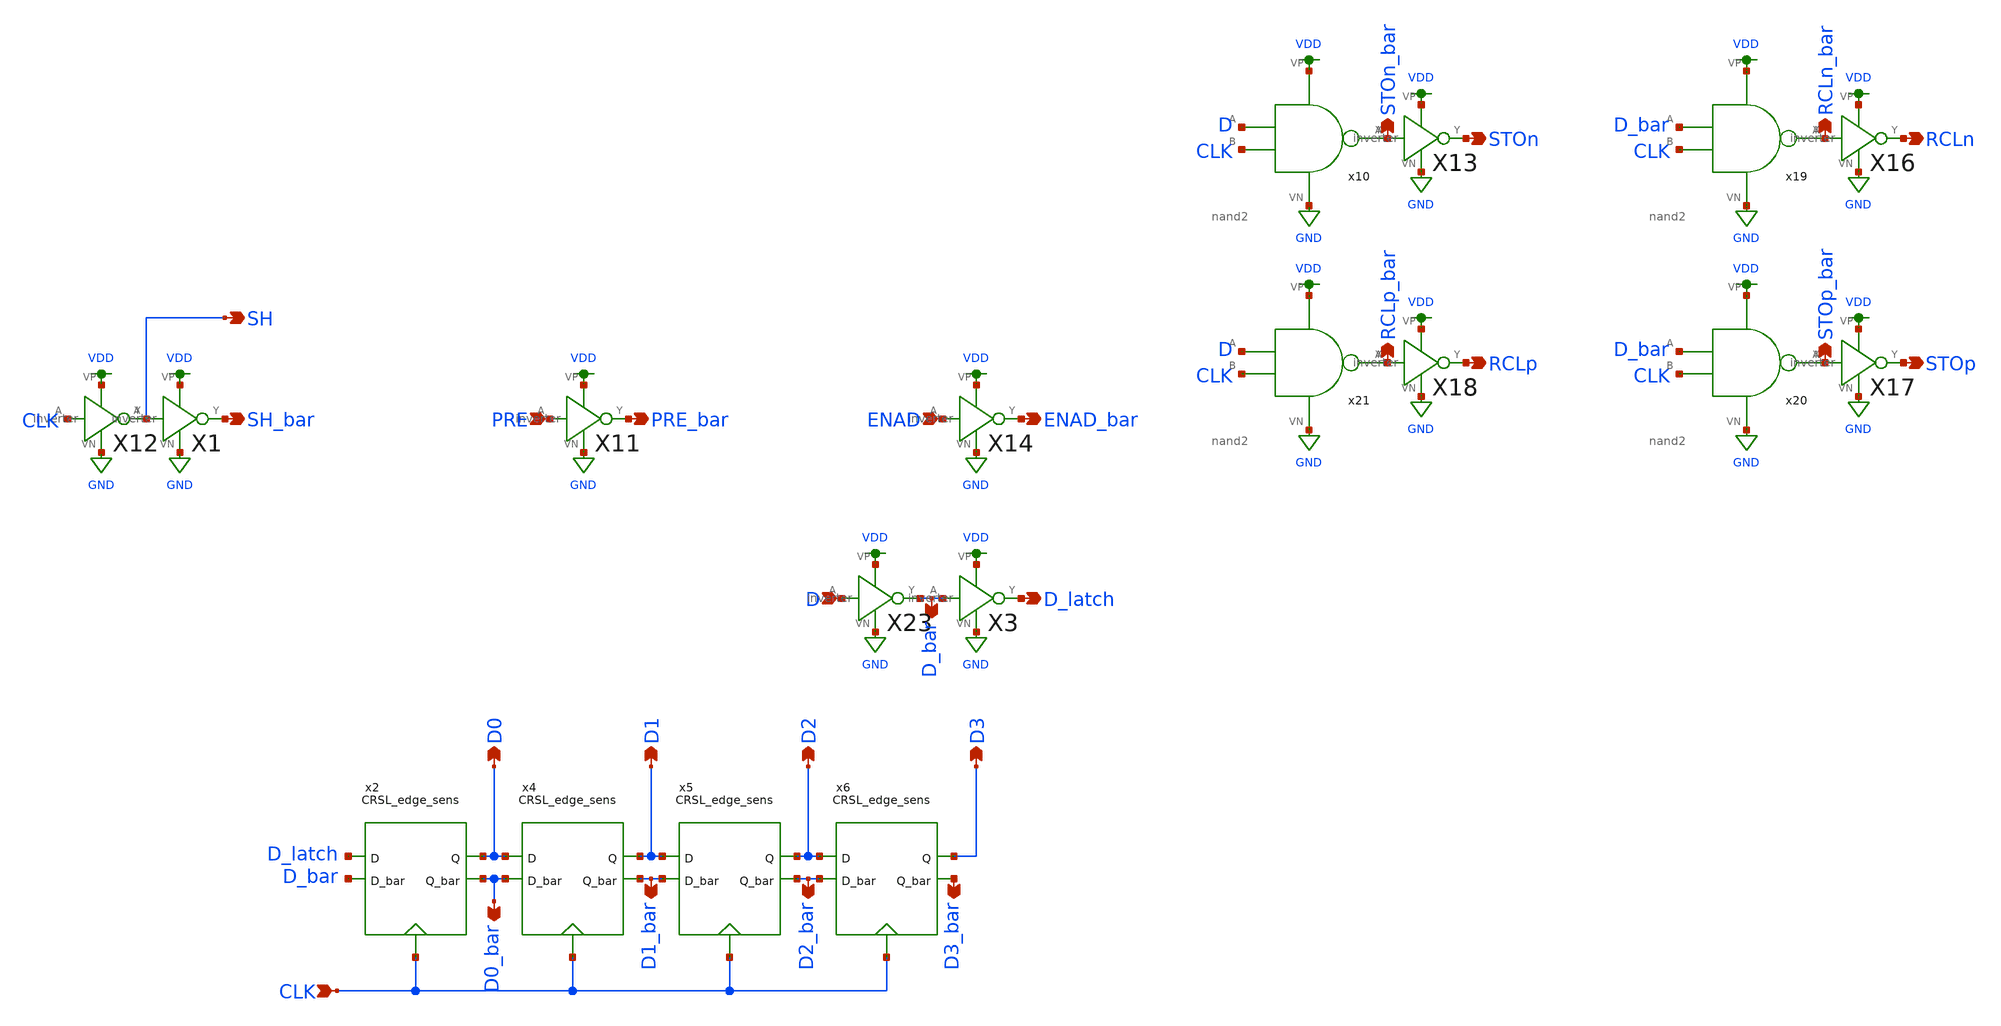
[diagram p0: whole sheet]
** sch_path: schematics/digital_control.sch
**.subckt digital_control D D1 D2 D3 CLK SH_bar SH PRE PRE_bar ENAD ENAD_bar STOp STOn RCLp RCLn
*+ D0_bar STOn_bar STOp_bar RCLn_bar RCLp_bar D0 D_bar D_latch D1_bar D2_bar D3_bar
*.ipin D
*.opin D1
*.opin D2
*.opin D3
*.ipin CLK
*.opin SH_bar
*.opin SH
*.ipin PRE
*.opin PRE_bar
*.ipin ENAD
*.opin ENAD_bar
*.opin STOp
*.opin STOn
*.opin RCLp
*.opin RCLn
*.opin D0_bar
*.opin STOn_bar
*.opin STOp_bar
*.opin RCLn_bar
*.opin RCLp_bar
*.opin D0
*.opin D_bar
*.opin D_latch
*.opin D1_bar
*.opin D2_bar
*.opin D3_bar
x4 CLK D1 D0 D1_bar D0_bar CRSL_edge_sens
x5 CLK D2 D1 D2_bar D1_bar CRSL_edge_sens
x6 CLK D3 D2 D3_bar D2_bar CRSL_edge_sens
x10 VDD CLK STOn_bar D GND nand2
X13 STOn_bar STOn VDD GND inverter
X16 RCLn_bar RCLn VDD GND inverter
X17 STOp_bar STOp VDD GND inverter
X18 RCLp_bar RCLp VDD GND inverter
x19 VDD CLK RCLn_bar D_bar GND nand2
x20 VDD CLK STOp_bar D_bar GND nand2
x21 VDD CLK RCLp_bar D GND nand2
X23 D D_bar VDD GND inverter
X12 CLK SH VDD GND inverter
X1 SH SH_bar VDD GND inverter
X11 PRE PRE_bar VDD GND inverter
X14 ENAD ENAD_bar VDD GND inverter
x2 CLK D0 D_latch D0_bar D_bar CRSL_edge_sens
X3 D_bar D_latch VDD GND inverter
**.ends

* expanding   symbol:  ../schematics/CRSL_edge_sens.sym # of pins=5
** sym_path: schematics/CRSL_edge_sens.sym
** sch_path: schematics/CRSL_edge_sens.sch
.subckt CRSL_edge_sens Phi Q D Q_bar D_bar
*.ipin D
*.ipin D_bar
*.opin Q
*.opin Q_bar
*.ipin Phi
XM14 Q_bar Q GND GND sky130_fd_pr__nfet_01v8 L=0.15 W=1 nf=1 ad='int((nf+1)/2) * W/nf * 0.29' as='int((nf+2)/2) * W/nf * 0.29'
+ pd='2*int((nf+1)/2) * (W/nf + 0.29)' ps='2*int((nf+2)/2) * (W/nf + 0.29)' nrd='0.29 / W' nrs='0.29 / W'
+ sa=0 sb=0 sd=0 mult=1 m=1
XM2 Q_bar Phi net3 GND sky130_fd_pr__nfet_01v8 L=0.15 W=1 nf=1 ad='int((nf+1)/2) * W/nf * 0.29' as='int((nf+2)/2) * W/nf * 0.29'
+ pd='2*int((nf+1)/2) * (W/nf + 0.29)' ps='2*int((nf+2)/2) * (W/nf + 0.29)' nrd='0.29 / W' nrs='0.29 / W'
+ sa=0 sb=0 sd=0 mult=1 m=1
XM6 Q Phi net2 GND sky130_fd_pr__nfet_01v8 L=0.15 W=1 nf=1 ad='int((nf+1)/2) * W/nf * 0.29' as='int((nf+2)/2) * W/nf * 0.29'
+ pd='2*int((nf+1)/2) * (W/nf + 0.29)' ps='2*int((nf+2)/2) * (W/nf + 0.29)' nrd='0.29 / W' nrs='0.29 / W'
+ sa=0 sb=0 sd=0 mult=1 m=1
XM7 net4 Phi GND GND sky130_fd_pr__nfet_01v8 L=0.15 W=4 nf=1 ad='int((nf+1)/2) * W/nf * 0.29' as='int((nf+2)/2) * W/nf * 0.29'
+ pd='2*int((nf+1)/2) * (W/nf + 0.29)' ps='2*int((nf+2)/2) * (W/nf + 0.29)' nrd='0.29 / W' nrs='0.29 / W'
+ sa=0 sb=0 sd=0 mult=1 m=1
XM8 net3 net2 net4 GND sky130_fd_pr__nfet_01v8 L=0.15 W=1 nf=1 ad='int((nf+1)/2) * W/nf * 0.29' as='int((nf+2)/2) * W/nf * 0.29'
+ pd='2*int((nf+1)/2) * (W/nf + 0.29)' ps='2*int((nf+2)/2) * (W/nf + 0.29)' nrd='0.29 / W' nrs='0.29 / W'
+ sa=0 sb=0 sd=0 mult=1 m=1
XM12 net3 net2 VDD VDD sky130_fd_pr__pfet_01v8 L=0.15 W=1 nf=1 ad='int((nf+1)/2) * W/nf * 0.29' as='int((nf+2)/2) * W/nf * 0.29'
+ pd='2*int((nf+1)/2) * (W/nf + 0.29)' ps='2*int((nf+2)/2) * (W/nf + 0.29)' nrd='0.29 / W' nrs='0.29 / W'
+ sa=0 sb=0 sd=0 mult=1 m=1
XM9 net2 net3 VDD VDD sky130_fd_pr__pfet_01v8 L=0.15 W=1 nf=1 ad='int((nf+1)/2) * W/nf * 0.29' as='int((nf+2)/2) * W/nf * 0.29'
+ pd='2*int((nf+1)/2) * (W/nf + 0.29)' ps='2*int((nf+2)/2) * (W/nf + 0.29)' nrd='0.29 / W' nrs='0.29 / W'
+ sa=0 sb=0 sd=0 mult=1 m=1
XM1 net1 Phi VDD VDD sky130_fd_pr__pfet_01v8 L=0.15 W=8 nf=1 ad='int((nf+1)/2) * W/nf * 0.29' as='int((nf+2)/2) * W/nf * 0.29'
+ pd='2*int((nf+1)/2) * (W/nf + 0.29)' ps='2*int((nf+2)/2) * (W/nf + 0.29)' nrd='0.29 / W' nrs='0.29 / W'
+ sa=0 sb=0 sd=0 mult=1 m=1
XM3 Q_bar Q net1 VDD sky130_fd_pr__pfet_01v8 L=0.15 W=1 nf=1 ad='int((nf+1)/2) * W/nf * 0.29' as='int((nf+2)/2) * W/nf * 0.29'
+ pd='2*int((nf+1)/2) * (W/nf + 0.29)' ps='2*int((nf+2)/2) * (W/nf + 0.29)' nrd='0.29 / W' nrs='0.29 / W'
+ sa=0 sb=0 sd=0 mult=1 m=1
XM4 Q Q_bar net1 VDD sky130_fd_pr__pfet_01v8 L=0.15 W=1 nf=1 ad='int((nf+1)/2) * W/nf * 0.29' as='int((nf+2)/2) * W/nf * 0.29'
+ pd='2*int((nf+1)/2) * (W/nf + 0.29)' ps='2*int((nf+2)/2) * (W/nf + 0.29)' nrd='0.29 / W' nrs='0.29 / W'
+ sa=0 sb=0 sd=0 mult=1 m=1
XM10 Q Q_bar GND GND sky130_fd_pr__nfet_01v8 L=0.15 W=1 nf=1 ad='int((nf+1)/2) * W/nf * 0.29' as='int((nf+2)/2) * W/nf * 0.29'
+ pd='2*int((nf+1)/2) * (W/nf + 0.29)' ps='2*int((nf+2)/2) * (W/nf + 0.29)' nrd='0.29 / W' nrs='0.29 / W'
+ sa=0 sb=0 sd=0 mult=1 m=1
XM5 net2 net3 net4 GND sky130_fd_pr__nfet_01v8 L=0.15 W=1 nf=1 ad='int((nf+1)/2) * W/nf * 0.29' as='int((nf+2)/2) * W/nf * 0.29'
+ pd='2*int((nf+1)/2) * (W/nf + 0.29)' ps='2*int((nf+2)/2) * (W/nf + 0.29)' nrd='0.29 / W' nrs='0.29 / W'
+ sa=0 sb=0 sd=0 mult=1 m=1
XM11 net3 Phi D_bar VDD sky130_fd_pr__pfet_01v8 L=0.15 W=1 nf=1 ad='int((nf+1)/2) * W/nf * 0.29' as='int((nf+2)/2) * W/nf * 0.29'
+ pd='2*int((nf+1)/2) * (W/nf + 0.29)' ps='2*int((nf+2)/2) * (W/nf + 0.29)' nrd='0.29 / W' nrs='0.29 / W'
+ sa=0 sb=0 sd=0 mult=1 m=1
XM15 net2 Phi D VDD sky130_fd_pr__pfet_01v8 L=0.15 W=1 nf=1 ad='int((nf+1)/2) * W/nf * 0.29' as='int((nf+2)/2) * W/nf * 0.29'
+ pd='2*int((nf+1)/2) * (W/nf + 0.29)' ps='2*int((nf+2)/2) * (W/nf + 0.29)' nrd='0.29 / W' nrs='0.29 / W'
+ sa=0 sb=0 sd=0 mult=1 m=1
.ends


* expanding   symbol:  ../schematics/nand2.sym # of pins=5
** sym_path: schematics/nand2.sym
** sch_path: schematics/nand2.sch
.subckt nand2 VP B Y A VN
*.iopin VP
*.iopin VN
*.ipin A
*.ipin B
*.opin Y
XM5 Y B VP VP sky130_fd_pr__pfet_01v8 L=0.15 W=1 nf=1 ad='int((nf+1)/2) * W/nf * 0.29' as='int((nf+2)/2) * W/nf * 0.29'
+ pd='2*int((nf+1)/2) * (W/nf + 0.29)' ps='2*int((nf+2)/2) * (W/nf + 0.29)' nrd='0.29 / W' nrs='0.29 / W'
+ sa=0 sb=0 sd=0 mult=1 m=1
XM2 Y A VP VP sky130_fd_pr__pfet_01v8 L=0.15 W=1 nf=1 ad='int((nf+1)/2) * W/nf * 0.29' as='int((nf+2)/2) * W/nf * 0.29'
+ pd='2*int((nf+1)/2) * (W/nf + 0.29)' ps='2*int((nf+2)/2) * (W/nf + 0.29)' nrd='0.29 / W' nrs='0.29 / W'
+ sa=0 sb=0 sd=0 mult=1 m=1
XM1 Y A net1 VN sky130_fd_pr__nfet_01v8 L=0.15 W=1 nf=1 ad='int((nf+1)/2) * W/nf * 0.29' as='int((nf+2)/2) * W/nf * 0.29'
+ pd='2*int((nf+1)/2) * (W/nf + 0.29)' ps='2*int((nf+2)/2) * (W/nf + 0.29)' nrd='0.29 / W' nrs='0.29 / W'
+ sa=0 sb=0 sd=0 mult=1 m=1
XM3 net1 B VN VN sky130_fd_pr__nfet_01v8 L=0.15 W=1 nf=1 ad='int((nf+1)/2) * W/nf * 0.29' as='int((nf+2)/2) * W/nf * 0.29'
+ pd='2*int((nf+1)/2) * (W/nf + 0.29)' ps='2*int((nf+2)/2) * (W/nf + 0.29)' nrd='0.29 / W' nrs='0.29 / W'
+ sa=0 sb=0 sd=0 mult=1 m=1
.ends


* expanding   symbol:  ../schematics/inverter.sym # of pins=4
** sym_path: schematics/inverter.sym
** sch_path: schematics/inverter.sch
.subckt inverter A Y VP VN
*.ipin A
*.iopin VP
*.iopin VN
*.opin Y
XM1 Y A VP VDD sky130_fd_pr__pfet_01v8 L=0.15 W=1 nf=1 ad='int((nf+1)/2) * W/nf * 0.29' as='int((nf+2)/2) * W/nf * 0.29'
+ pd='2*int((nf+1)/2) * (W/nf + 0.29)' ps='2*int((nf+2)/2) * (W/nf + 0.29)' nrd='0.29 / W' nrs='0.29 / W'
+ sa=0 sb=0 sd=0 mult=1 m=1
XM2 Y A VN GND sky130_fd_pr__nfet_01v8 L=0.15 W=1 nf=1 ad='int((nf+1)/2) * W/nf * 0.29' as='int((nf+2)/2) * W/nf * 0.29'
+ pd='2*int((nf+1)/2) * (W/nf + 0.29)' ps='2*int((nf+2)/2) * (W/nf + 0.29)' nrd='0.29 / W' nrs='0.29 / W'
+ sa=0 sb=0 sd=0 mult=1 m=1
.ends

.GLOBAL GND
.GLOBAL VDD
.end
